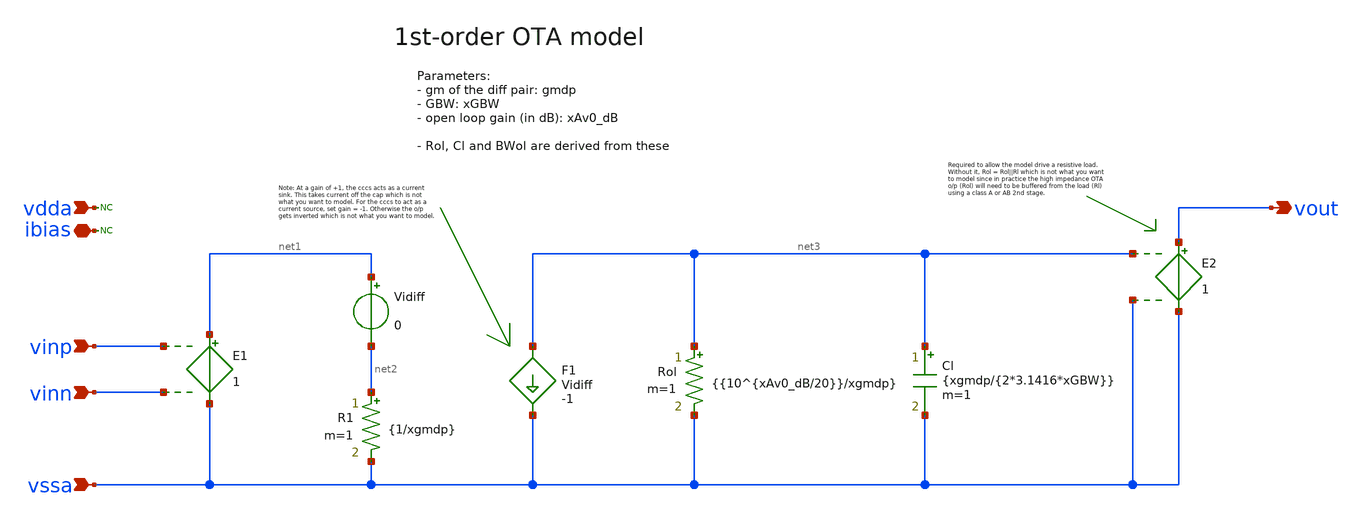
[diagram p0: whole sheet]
** sch_path: Design_Review_1/Testbench_4_tb_sunrise_opamp/OTA_ideal_order1_element.sch
**.subckt OTA_ideal_order1_element ibias vdda vssa vinp vinn vout
*.iopin ibias
*.ipin vdda
*.ipin vssa
*.ipin vinp
*.ipin vinn
*.opin vout
* noconn vdda
* noconn ibias
F1 net3 vssa Vidiff -1
E1 net1 vssa vinp vinn 1
Vidiff net1 net2 0
R1 net2 vssa {1/xgmdp} m=1
Cl net3 vssa {xgmdp/{2*3.1416*xGBW}} m=1
Rol net3 vssa {{10^{xAv0_dB/20}}/xgmdp} m=1
E2 vout vssa net3 vssa 1
**.ends
.end
